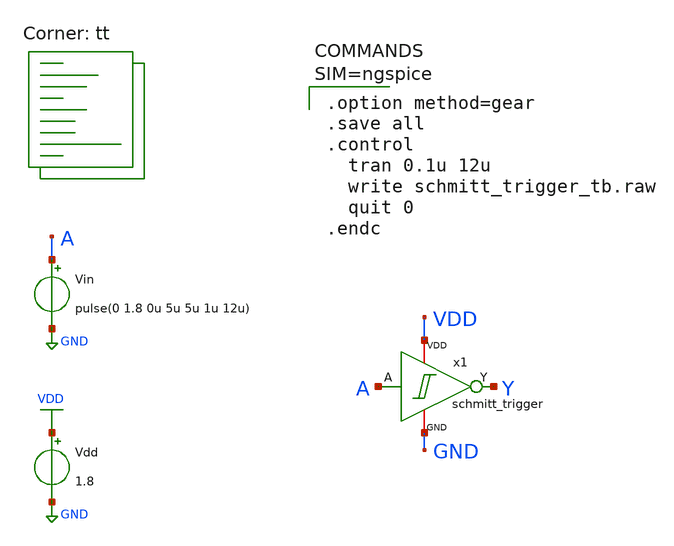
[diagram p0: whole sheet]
** sch_path: design/xschem/schmitt_trigger_tb.sch
**.subckt schmitt_trigger_tb
x1 A Y VDD GND schmitt_trigger
Vdd VDD GND 1.8
Vin A GND pulse(0 1.8 0u 5u 5u 1u 12u)
**** begin user architecture code


.option method=gear
.save all
.control
  tran 0.1u 12u
  write schmitt_trigger_tb.raw
  quit 0
.endc


.lib $::SKYWATER_MODELS/sky130.lib.spice tt
**** end user architecture code
**.ends

* expanding   symbol:  schmitt_trigger.sym # of pins=4
** sym_path: design/xschem/schmitt_trigger.sym
** sch_path: design/xschem/schmitt_trigger.sch
.subckt schmitt_trigger A Y VDD GND
*.ipin A
*.opin Y
*.iopin VDD
*.iopin GND
XM3 net2 A GND GND sky130_fd_pr__nfet_01v8 L=0.15 W=0.65 nf=1 ad='int((nf+1)/2) * W/nf * 0.29' as='int((nf+2)/2) * W/nf * 0.29'
+ pd='2*int((nf+1)/2) * (W/nf + 0.29)' ps='2*int((nf+2)/2) * (W/nf + 0.29)' nrd='0.29 / W' nrs='0.29 / W'
+ sa=0 sb=0 sd=0 mult=1 m=1
XM1 Y A net2 GND sky130_fd_pr__nfet_01v8 L=0.15 W=0.65 nf=1 ad='int((nf+1)/2) * W/nf * 0.29' as='int((nf+2)/2) * W/nf * 0.29'
+ pd='2*int((nf+1)/2) * (W/nf + 0.29)' ps='2*int((nf+2)/2) * (W/nf + 0.29)' nrd='0.29 / W' nrs='0.29 / W'
+ sa=0 sb=0 sd=0 mult=1 m=1
XM7 VDD Y net2 GND sky130_fd_pr__nfet_01v8 L=0.15 W=0.42 nf=1 ad='int((nf+1)/2) * W/nf * 0.29' as='int((nf+2)/2) * W/nf * 0.29'
+ pd='2*int((nf+1)/2) * (W/nf + 0.29)' ps='2*int((nf+2)/2) * (W/nf + 0.29)' nrd='0.29 / W' nrs='0.29 / W'
+ sa=0 sb=0 sd=0 mult=1 m=1
XM4 net1 A VDD VDD sky130_fd_pr__pfet_01v8 L=0.15 W=1 nf=1 ad='int((nf+1)/2) * W/nf * 0.29' as='int((nf+2)/2) * W/nf * 0.29'
+ pd='2*int((nf+1)/2) * (W/nf + 0.29)' ps='2*int((nf+2)/2) * (W/nf + 0.29)' nrd='0.29 / W' nrs='0.29 / W'
+ sa=0 sb=0 sd=0 mult=1 m=1
XM2 Y A net1 VDD sky130_fd_pr__pfet_01v8 L=0.15 W=1 nf=1 ad='int((nf+1)/2) * W/nf * 0.29' as='int((nf+2)/2) * W/nf * 0.29'
+ pd='2*int((nf+1)/2) * (W/nf + 0.29)' ps='2*int((nf+2)/2) * (W/nf + 0.29)' nrd='0.29 / W' nrs='0.29 / W'
+ sa=0 sb=0 sd=0 mult=1 m=1
XM5 GND Y net1 VDD sky130_fd_pr__pfet_01v8 L=0.15 W=0.82 nf=1 ad='int((nf+1)/2) * W/nf * 0.29' as='int((nf+2)/2) * W/nf * 0.29'
+ pd='2*int((nf+1)/2) * (W/nf + 0.29)' ps='2*int((nf+2)/2) * (W/nf + 0.29)' nrd='0.29 / W' nrs='0.29 / W'
+ sa=0 sb=0 sd=0 mult=1 m=1
.ends

.GLOBAL VDD
.GLOBAL GND
.end
